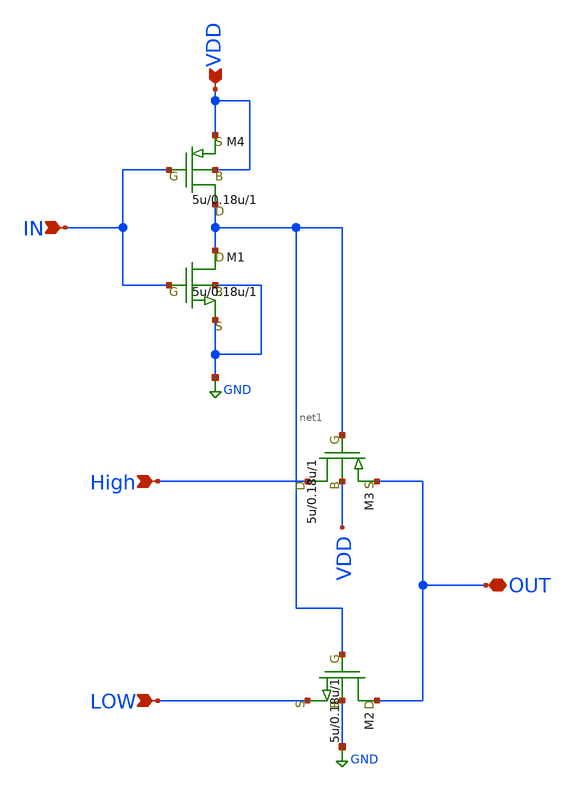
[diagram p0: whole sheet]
** sch_path: LR_Work3/Report_1003/SEL_1003.sch
**.subckt SEL_1003 High LOW IN VDD OUT
*.ipin High
*.ipin LOW
*.ipin IN
*.ipin VDD
*.iopin OUT
M4 net1 IN VDD VDD p3.0 w=5u l=0.18u as=0 ps=0 ad=0 pd=0 m=1
M1 net1 IN GND GND n3.0 w=5u l=0.18u as=0 ps=0 ad=0 pd=0 m=1
M2 OUT net1 LOW GND n3.0 w=5u l=0.18u as=0 ps=0 ad=0 pd=0 m=1
M3 High net1 OUT VDD p3.0 w=5u l=0.18u as=0 ps=0 ad=0 pd=0 m=1
**.ends
.GLOBAL GND
.end
